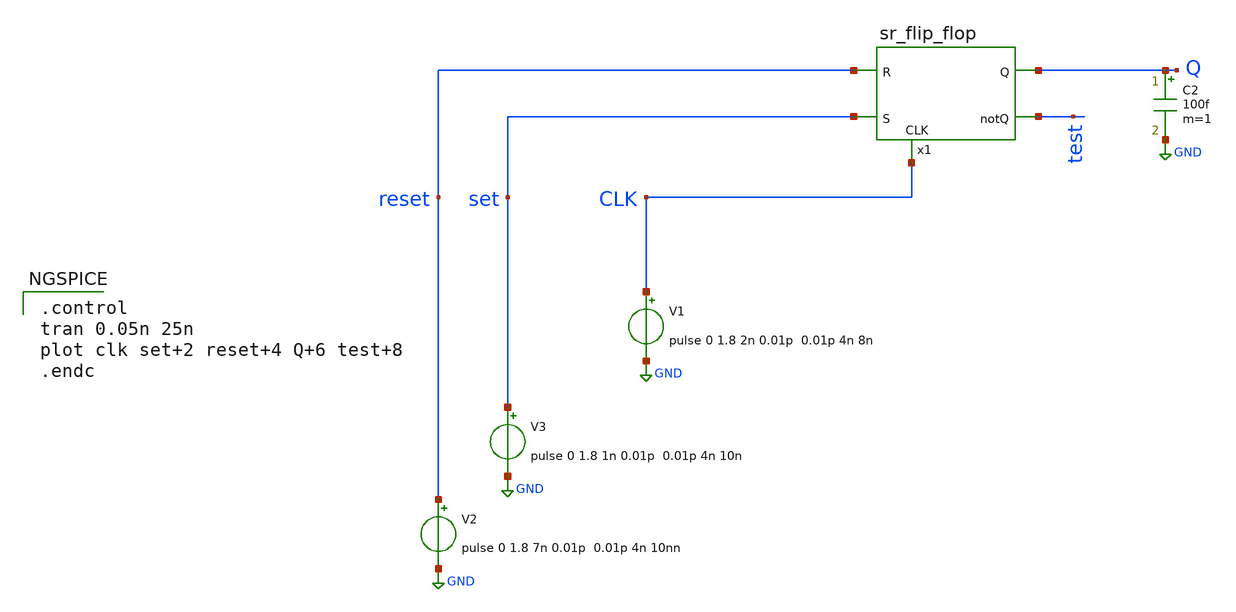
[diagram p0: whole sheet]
** sch_path: Circuiti/flipflop_demos.sch
**.subckt flipflop_demos
V1 CLK GND pulse 0 1.8 2n 0.01p 0.01p 4n 8n
V2 reset GND pulse 0 1.8 7n 0.01p 0.01p 4n 10nn
V3 set GND pulse 0 1.8 1n 0.01p 0.01p 4n 10n
x1 reset Q CLK test set sr_flip_flop
C2 Q GND 100f m=1
**** begin user architecture code


.lib /home/matteo/xschem_downloads/skywater-pdk/libraries/sky130_fd_pr_ngspice/latest/models/sky130.lib.spice tt

*.include /home/matteo/xschem_downloads/skywater-pdk/libraries/sky130_fd_pr_ngspice/latest/cells/nfet_01v8/sky130_fd_pr__nfet_01v8__tt.corner.spice

.param mc_mm_switch=0
.param mc_pr_switch=1



.control
tran 0.05n 25n
plot clk set+2 reset+4 Q+6 test+8
.endc


**** end user architecture code
**.ends

* expanding   symbol:  /home/matteo/Documenti/tesi/Circuiti/latches_sch_sym/sr_flip_flop.sym # of
*+ pins=5
** sym_path: Circuiti/latches_sch_sym/sr_flip_flop.sym
** sch_path: Circuiti/latches_sch_sym/sr_flip_flop.sch
.subckt sr_flip_flop R Q CLK notQ S
*.ipin R
*.ipin S
*.opin Q
*.opin notQ
*.ipin CLK
x1 net2 Q notQ nor_2
x2 Q notQ net1 nor_2
x3 net3 net1 S and_2
x4 R net2 net3 and_2
x5 CLK net4 not
x6 CLK net3 net4 and_2
C1 net4 GND 1.5p m=1
.ends


* expanding   symbol:  /home/matteo/Documenti/tesi/Circuiti/logic_gates_sch_sym/nor_2.sym # of
*+ pins=3
** sym_path: Circuiti/logic_gates_sch_sym/nor_2.sym
** sch_path: Circuiti/logic_gates_sch_sym/nor_2.sch
.subckt nor_2 A Y B
*.opin Y
*.ipin A
*.ipin B
XM1 Y B GND GND sky130_fd_pr__nfet_01v8 L=0.45 W=1 nf=1 ad='int((nf+1)/2) * W/nf * 0.29' as='int((nf+2)/2) * W/nf * 0.29'
+ pd='2*int((nf+1)/2) * (W/nf + 0.29)' ps='2*int((nf+2)/2) * (W/nf + 0.29)' nrd='0.29 / W' nrs='0.29 / W'
+ sa=0 sb=0 sd=0 mult=1 m=1
XM3 Y B net1 VDD sky130_fd_pr__pfet_01v8 L=0.15 W=4.8 nf=1 ad='int((nf+1)/2) * W/nf * 0.29' as='int((nf+2)/2) * W/nf * 0.29'
+ pd='2*int((nf+1)/2) * (W/nf + 0.29)' ps='2*int((nf+2)/2) * (W/nf + 0.29)' nrd='0.29 / W' nrs='0.29 / W'
+ sa=0 sb=0 sd=0 mult=1 m=1
XM4 net1 A Vdd VDD sky130_fd_pr__pfet_01v8 L=0.15 W=4.8 nf=1 ad='int((nf+1)/2) * W/nf * 0.29' as='int((nf+2)/2) * W/nf * 0.29'
+ pd='2*int((nf+1)/2) * (W/nf + 0.29)' ps='2*int((nf+2)/2) * (W/nf + 0.29)' nrd='0.29 / W' nrs='0.29 / W'
+ sa=0 sb=0 sd=0 mult=1 m=1
XM2 Y A GND GND sky130_fd_pr__nfet_01v8 L=0.45 W=1 nf=1 ad='int((nf+1)/2) * W/nf * 0.29' as='int((nf+2)/2) * W/nf * 0.29'
+ pd='2*int((nf+1)/2) * (W/nf + 0.29)' ps='2*int((nf+2)/2) * (W/nf + 0.29)' nrd='0.29 / W' nrs='0.29 / W'
+ sa=0 sb=0 sd=0 mult=1 m=1
.ends


* expanding   symbol:  /home/matteo/Documenti/tesi/Circuiti/logic_gates_sch_sym/and_2.sym # of
*+ pins=3
** sym_path: Circuiti/logic_gates_sch_sym/and_2.sym
** sch_path: Circuiti/logic_gates_sch_sym/and_2.sch
.subckt and_2 A Y B
*.ipin B
*.ipin A
*.opin Y
x1 A net1 B nand_2
x2 net1 Y not
.ends


* expanding   symbol:  /home/matteo/Documenti/tesi/Circuiti/logic_gates_sch_sym/not.sym # of pins=2
** sym_path: Circuiti/logic_gates_sch_sym/not.sym
** sch_path: Circuiti/logic_gates_sch_sym/not.sch
.subckt not A Y
*.ipin A
*.opin Y
XM1 Y A GND GND sky130_fd_pr__nfet_01v8 L=0.45 W=1 nf=1 ad='int((nf+1)/2) * W/nf * 0.29' as='int((nf+2)/2) * W/nf * 0.29'
+ pd='2*int((nf+1)/2) * (W/nf + 0.29)' ps='2*int((nf+2)/2) * (W/nf + 0.29)' nrd='0.29 / W' nrs='0.29 / W'
+ sa=0 sb=0 sd=0 mult=1 m=1
XM2 Y A Vdd VDD sky130_fd_pr__pfet_01v8 L=0.45 W=4.8 nf=1 ad='int((nf+1)/2) * W/nf * 0.29' as='int((nf+2)/2) * W/nf * 0.29'
+ pd='2*int((nf+1)/2) * (W/nf + 0.29)' ps='2*int((nf+2)/2) * (W/nf + 0.29)' nrd='0.29 / W' nrs='0.29 / W'
+ sa=0 sb=0 sd=0 mult=1 m=1
.ends


* expanding   symbol:  /home/matteo/Documenti/tesi/Circuiti/logic_gates_sch_sym/nand_2.sym # of
*+ pins=3
** sym_path: Circuiti/logic_gates_sch_sym/nand_2.sym
** sch_path: Circuiti/logic_gates_sch_sym/nand_2.sch
.subckt nand_2 A Y B
*.ipin A
*.ipin B
*.opin Y
XM1 Y A net1 GND sky130_fd_pr__nfet_01v8 L=0.15 W=1 nf=1 ad='int((nf+1)/2) * W/nf * 0.29' as='int((nf+2)/2) * W/nf * 0.29'
+ pd='2*int((nf+1)/2) * (W/nf + 0.29)' ps='2*int((nf+2)/2) * (W/nf + 0.29)' nrd='0.29 / W' nrs='0.29 / W'
+ sa=0 sb=0 sd=0 mult=1 m=1
XM3 Y B Vdd VDD sky130_fd_pr__pfet_01v8 L=0.45 W=4.8 nf=1 ad='int((nf+1)/2) * W/nf * 0.29' as='int((nf+2)/2) * W/nf * 0.29'
+ pd='2*int((nf+1)/2) * (W/nf + 0.29)' ps='2*int((nf+2)/2) * (W/nf + 0.29)' nrd='0.29 / W' nrs='0.29 / W'
+ sa=0 sb=0 sd=0 mult=1 m=1
XM4 Y A Vdd VDD sky130_fd_pr__pfet_01v8 L=0.45 W=4.8 nf=1 ad='int((nf+1)/2) * W/nf * 0.29' as='int((nf+2)/2) * W/nf * 0.29'
+ pd='2*int((nf+1)/2) * (W/nf + 0.29)' ps='2*int((nf+2)/2) * (W/nf + 0.29)' nrd='0.29 / W' nrs='0.29 / W'
+ sa=0 sb=0 sd=0 mult=1 m=1
XM2 net1 B GND GND sky130_fd_pr__nfet_01v8 L=0.15 W=1 nf=1 ad='int((nf+1)/2) * W/nf * 0.29' as='int((nf+2)/2) * W/nf * 0.29'
+ pd='2*int((nf+1)/2) * (W/nf + 0.29)' ps='2*int((nf+2)/2) * (W/nf + 0.29)' nrd='0.29 / W' nrs='0.29 / W'
+ sa=0 sb=0 sd=0 mult=1 m=1
.ends

.GLOBAL GND
.GLOBAL Vdd
.end
